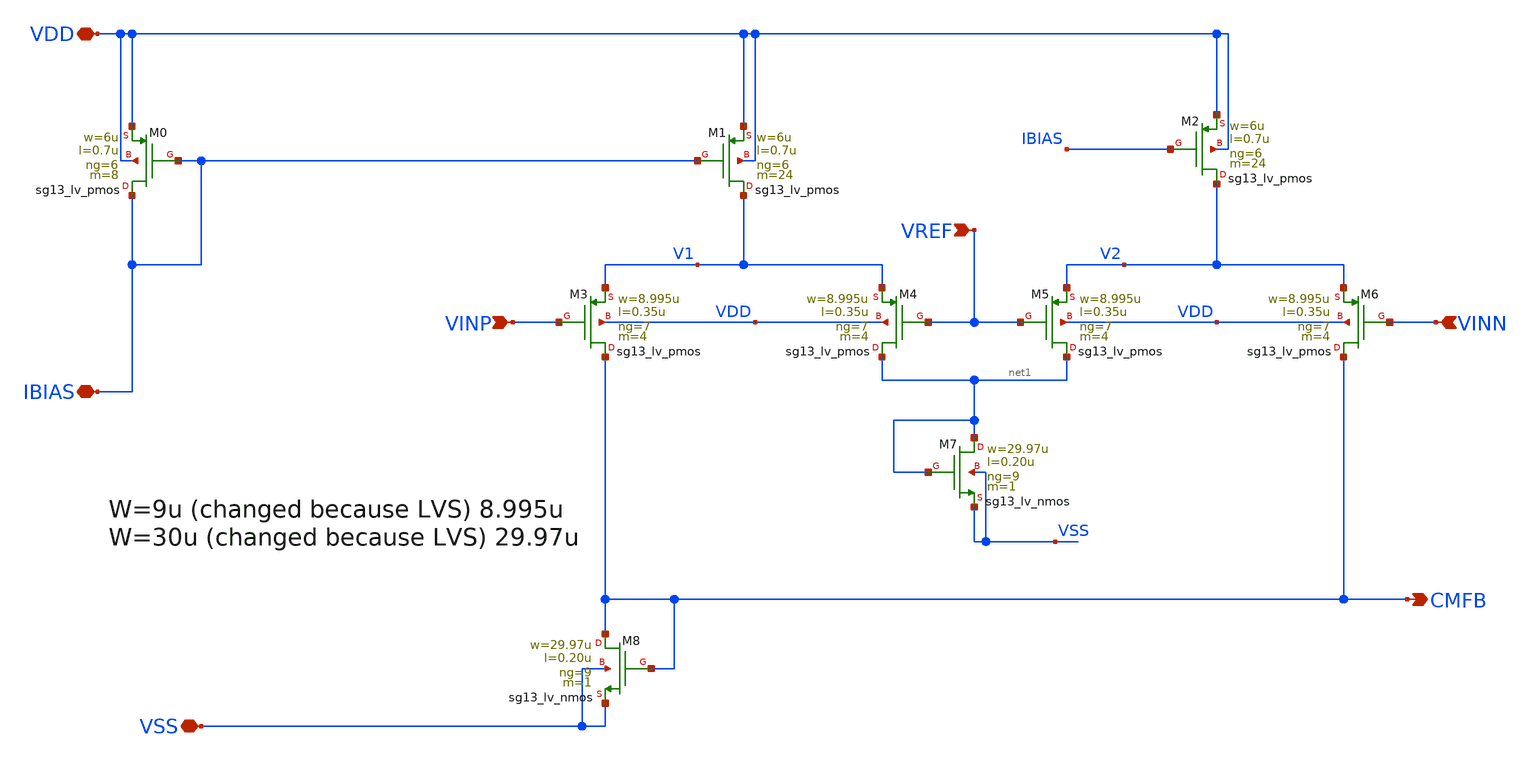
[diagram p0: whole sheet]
** sch_path: OTA_Telescopic_v3/Schematics_and_Symbols/OTA_Telescopic_CMFB.sch
**.subckt OTA_Telescopic_CMFB VDD VSS CMFB VREF IBIAS VINP VINN
*.iopin VDD
*.iopin VSS
*.opin CMFB
*.ipin VREF
*.iopin IBIAS
*.ipin VINP
*.ipin VINN
XM0 IBIAS IBIAS VDD VDD sg13_lv_pmos w=6u l=0.7u ng=6 m=8 mm_ok=1
XM1 V1 IBIAS VDD VDD sg13_lv_pmos w=6u l=0.7u ng=6 m=24 mm_ok=1
XM2 V2 IBIAS VDD VDD sg13_lv_pmos w=6u l=0.7u ng=6 m=24 mm_ok=1
XM3 CMFB VINP V1 VDD sg13_lv_pmos w=8.995u l=0.35u ng=7 m=4 mm_ok=1
XM4 net1 VREF V1 VDD sg13_lv_pmos w=8.995u l=0.35u ng=7 m=4 mm_ok=1
XM5 net1 VREF V2 VDD sg13_lv_pmos w=8.995u l=0.35u ng=7 m=4 mm_ok=1
XM6 CMFB VINN V2 VDD sg13_lv_pmos w=8.995u l=0.35u ng=7 m=4 mm_ok=1
XM7 net1 net1 VSS VSS sg13_lv_nmos w=29.97u l=0.20u ng=9 m=1 mm_ok=1
XM8 CMFB CMFB VSS VSS sg13_lv_nmos w=29.97u l=0.20u ng=9 m=1 mm_ok=1
**.ends
.end
